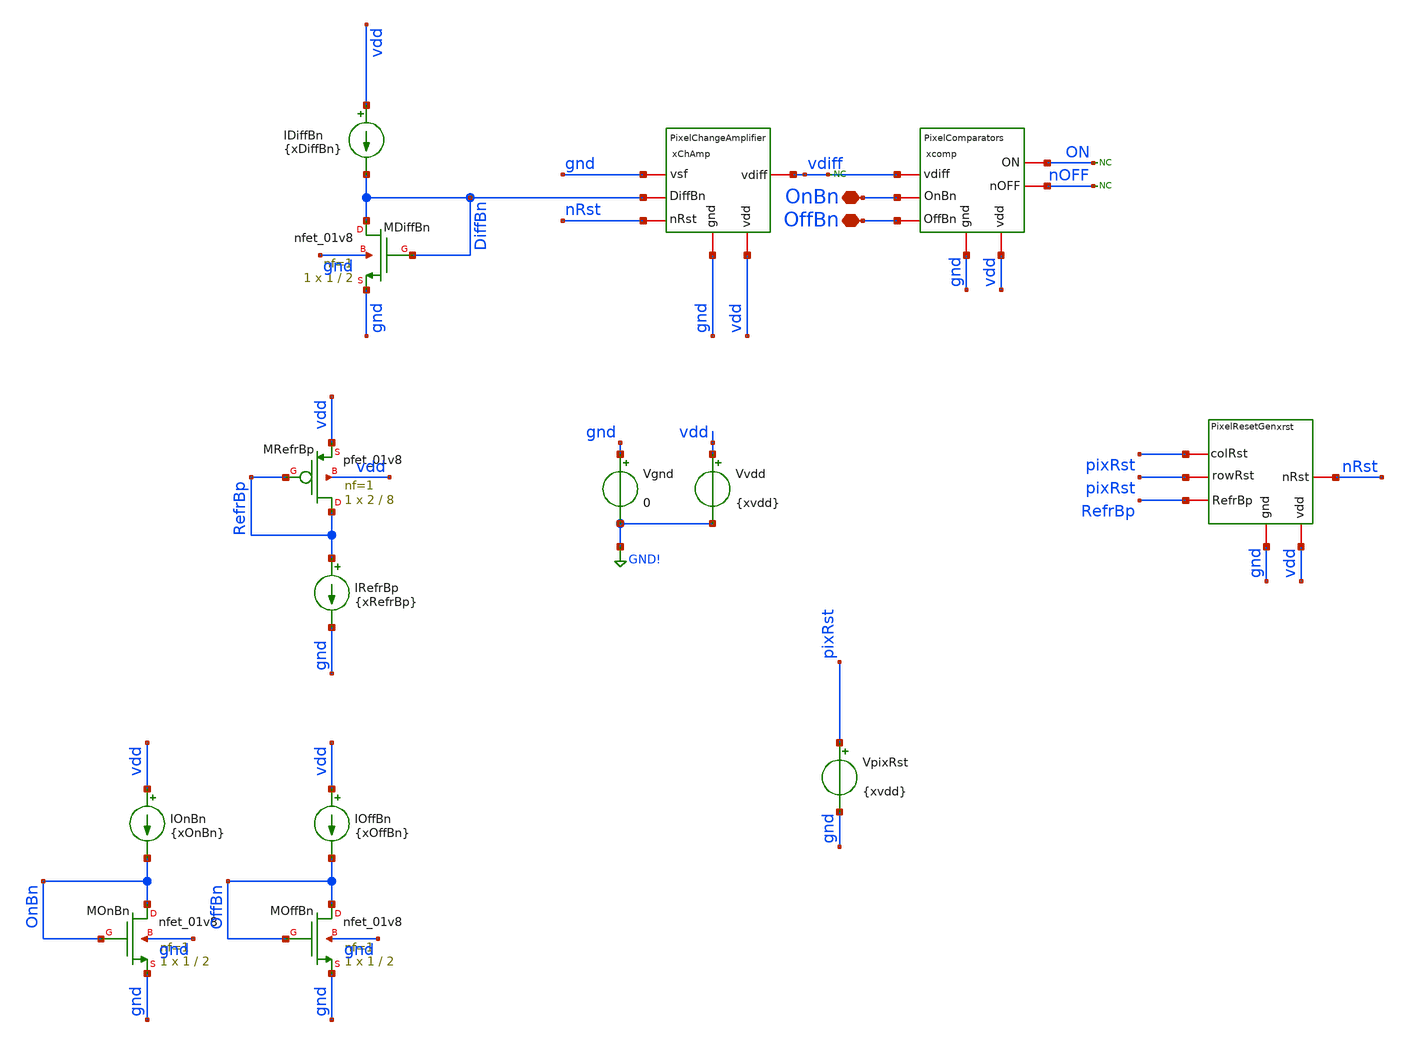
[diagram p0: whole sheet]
** sch_path: analog/xschem/tb_PixelReset_tran.sch
**.subckt tb_PixelReset_tran OnBn OffBn
*.iopin OnBn
*.iopin OffBn
Vgnd gnd GND! 0
Vvdd vdd GND! {xvdd}
xChAmp vdd DiffBn gnd gnd vdiff nRst PixelChangeAmplifier
XMDiffBn DiffBn DiffBn gnd gnd sky130_fd_pr__nfet_01v8 L=2 W=1 nf=1 ad='int((1 + 1)/2) * 1 / 1 * 0.29'
+ as='int((1 + 2)/2) * 1 / 1 * 0.29' pd='2*int((1 + 1)/2) * (1 / 1 + 0.29)' ps='2*int((1 + 2)/2) * (1 / 1 + 0.29)'
+ nrd='0.29 / 1 ' nrs='0.29 / 1 ' sa=0 sb=0 sd=0 mult=1 m=1
IDiffBn vdd DiffBn {xDiffBn}
* noconn vdiff
xcomp vdd OnBn gnd vdiff ON OffBn nOFF PixelComparators
xrst pixRst gnd pixRst nRst RefrBp vdd PixelResetGen
IRefrBp RefrBp gnd {xRefrBp}
XMRefrBp RefrBp RefrBp vdd vdd sky130_fd_pr__pfet_01v8 L=8 W=2 nf=1 ad='int((1 + 1)/2) * 2 / 1 * 0.29'
+ as='int((1 + 2)/2) * 2 / 1 * 0.29' pd='2*int((1 + 1)/2) * (2 / 1 + 0.29)' ps='2*int((1 + 2)/2) * (2 / 1 + 0.29)'
+ nrd='0.29 / 2 ' nrs='0.29 / 2 ' sa=0 sb=0 sd=0 mult=1 m=1
XMOnBn OnBn OnBn gnd gnd sky130_fd_pr__nfet_01v8 L=2 W=1 nf=1 ad='int((1 + 1)/2) * 1 / 1 * 0.29' as='int((1 + 2)/2) * 1 / 1 * 0.29'
+ pd='2*int((1 + 1)/2) * (1 / 1 + 0.29)' ps='2*int((1 + 2)/2) * (1 / 1 + 0.29)' nrd='0.29 / 1 ' nrs='0.29 / 1 '
+ sa=0 sb=0 sd=0 mult=1 m=1
IOnBn vdd OnBn {xOnBn}
XMOffBn OffBn OffBn gnd gnd sky130_fd_pr__nfet_01v8 L=2 W=1 nf=1 ad='int((1 + 1)/2) * 1 / 1 * 0.29' as='int((1 + 2)/2) * 1 / 1 * 0.29'
+ pd='2*int((1 + 1)/2) * (1 / 1 + 0.29)' ps='2*int((1 + 2)/2) * (1 / 1 + 0.29)' nrd='0.29 / 1 ' nrs='0.29 / 1 '
+ sa=0 sb=0 sd=0 mult=1 m=1
IOffBn vdd OffBn {xOffBn}
VpixRst pixRst gnd {xvdd}
* noconn ON
* noconn nOFF
**** begin user architecture code

** opencircuitdesign pdks install
.lib $::SKYWATER_MODELS/sky130.lib.spice tt



.temp 27

.option gmin=1e-16 abstol=1e-15 vntol=1e-9 reltol=1e-4 chgtol=1e-16
.option method=gear maxord=2 trtol=1
.option itl1=500 itl2=200 itl4=50
.option gminsteps=200 srcsteps=200

.param xvdd = 1.8
.param xRefrBp = 4n
.param xDiffBn = 10n
.param xOnBn = 100n
.param xOffBn = 1n

.param xvsf = 0.7

.save all
.save @m.xchamp.xmrst.msky130_fd_pr__pfet_01v8_hvt[id]
.save @m.xchamp.xmrst.msky130_fd_pr__pfet_01v8_hvt[ibd]
.save @m.xchamp.xmrst.msky130_fd_pr__pfet_01v8_hvt[ibs]
.save @m.xchamp.xmrst.msky130_fd_pr__pfet_01v8_hvt[igidl]
.save @m.xchamp.xmrst.msky130_fd_pr__pfet_01v8_hvt[igisl]

.control
** Phase 1: initial reset (VpixRst = xvdd from schematic)
stop when time > 1m
tran 100u 50 uic
let vdd_val = v(vdd)[length(v(vdd))-1]
echo
echo '=== Phase 1: initial reset complete (t=1ms) ==='

** Phase 2: release reset, run until ON fires
alter vpixrst = 0
delete all
let on_thresh = 0.9 * vdd_val
stop when v(on) > $&on_thresh
resume

let t_on_event = time[length(time)-1]
echo
echo '=== Phase 2: ON event detected ==='
print t_on_event

** Phase 3: trigger second reset for 10us
alter vpixrst = $&vdd_val
delete all
let t_rst2_end = t_on_event + 10u
stop when time > $&t_rst2_end
resume
echo
echo '=== Phase 3: second reset complete (10us pulse) ==='

** Phase 4: release second reset, run 0.5s more
alter vpixrst = 0
delete all
let t_final = t_on_event + 0.5
stop when time > $&t_final
resume
echo
echo '=== Phase 4: post-reset observation complete ==='

write tb_PixelReset_tran.raw
echo 'Raw file written. Running Python analysis...'
shell python3
+ /home/rpgraca/research/projects/telluride/2025/nic_eventcam/nic2025_openDVS/analog/xschem/tb_PixelReset_tran.py tb_PixelReset_tran.raw
.endc


**** end user architecture code
**.ends

* expanding   symbol:  PixelChangeAmplifier.sym # of pins=6
** sym_path: analog/xschem/PixelChangeAmplifier.sym
** sch_path: analog/xschem/PixelChangeAmplifier.sch
.subckt PixelChangeAmplifier vdd DiffBn gnd vsf vdiff nRst
*.iopin DiffBn
*.iopin vsf
*.iopin vdd
*.iopin gnd
*.iopin vdiff
*.iopin nRst
XC1 vsf vd sky130_fd_pr__cap_mim_m3_1 W=1 L=1 MF=40 m=40
XC2 vd vdiff sky130_fd_pr__cap_mim_m3_1 W=1 L=1 MF=2 m=2
XMchAmpBias vdiff DiffBn gnd gnd sky130_fd_pr__nfet_01v8 L=2 W=2 nf=1 ad='int((1 + 1)/2) * 2 / 1 * 0.29'
+ as='int((1 + 2)/2) * 2 / 1 * 0.29' pd='2*int((1 + 1)/2) * (2 / 1 + 0.29)' ps='2*int((1 + 2)/2) * (2 / 1 + 0.29)'
+ nrd='0.29 / 2 ' nrs='0.29 / 2 ' sa=0 sb=0 sd=0 mult=1 m=1
XMrst vdiff nRst vd vdd sky130_fd_pr__pfet_01v8_hvt L=0.3 W=1 nf=1 ad='int((1 + 1)/2) * 1 / 1 * 0.29'
+ as='int((1 + 2)/2) * 1 / 1 * 0.29' pd='2*int((1 + 1)/2) * (1 / 1 + 0.29)' ps='2*int((1 + 2)/2) * (1 / 1 + 0.29)'
+ nrd='0.29 / 1 ' nrs='0.29 / 1 ' sa=0 sb=0 sd=0 mult=1 m=1
XMchAmp vdiff vd vdd vdd sky130_fd_pr__pfet_01v8_hvt L=2 W=2 nf=1 ad='int((1 + 1)/2) * 2 / 1 * 0.29'
+ as='int((1 + 2)/2) * 2 / 1 * 0.29' pd='2*int((1 + 1)/2) * (2 / 1 + 0.29)' ps='2*int((1 + 2)/2) * (2 / 1 + 0.29)'
+ nrd='0.29 / 2 ' nrs='0.29 / 2 ' sa=0 sb=0 sd=0 mult=1 m=1
.ends


* expanding   symbol:  PixelComparators.sym # of pins=7
** sym_path: analog/xschem/PixelComparators.sym
** sch_path: analog/xschem/PixelComparators.sch
.subckt PixelComparators vdd OnBn gnd vdiff ON OffBn nOFF
*.iopin OnBn
*.iopin OffBn
*.iopin vdd
*.iopin vdiff
*.iopin gnd
*.iopin ON
*.iopin nOFF
XMonBias ON OnBn gnd gnd sky130_fd_pr__nfet_01v8 L=2 W=2 nf=1 ad='int((1 + 1)/2) * 2 / 1 * 0.29' as='int((1 + 2)/2) * 2 / 1 * 0.29'
+ pd='2*int((1 + 1)/2) * (2 / 1 + 0.29)' ps='2*int((1 + 2)/2) * (2 / 1 + 0.29)' nrd='0.29 / 2 ' nrs='0.29 / 2 '
+ sa=0 sb=0 sd=0 mult=1 m=1
XMoffBias nOFF OffBn gnd gnd sky130_fd_pr__nfet_01v8 L=2 W=2 nf=1 ad='int((1 + 1)/2) * 2 / 1 * 0.29'
+ as='int((1 + 2)/2) * 2 / 1 * 0.29' pd='2*int((1 + 1)/2) * (2 / 1 + 0.29)' ps='2*int((1 + 2)/2) * (2 / 1 + 0.29)'
+ nrd='0.29 / 2 ' nrs='0.29 / 2 ' sa=0 sb=0 sd=0 mult=1 m=1
XMon ON vdiff vdd vdd sky130_fd_pr__pfet_01v8_hvt L=2 W=2 nf=1 ad='int((1 + 1)/2) * 2 / 1 * 0.29' as='int((1 + 2)/2) * 2 / 1 * 0.29'
+ pd='2*int((1 + 1)/2) * (2 / 1 + 0.29)' ps='2*int((1 + 2)/2) * (2 / 1 + 0.29)' nrd='0.29 / 2 ' nrs='0.29 / 2 '
+ sa=0 sb=0 sd=0 mult=1 m=1
XMoff nOFF vdiff vdd vdd sky130_fd_pr__pfet_01v8_hvt L=2 W=2 nf=1 ad='int((1 + 1)/2) * 2 / 1 * 0.29'
+ as='int((1 + 2)/2) * 2 / 1 * 0.29' pd='2*int((1 + 1)/2) * (2 / 1 + 0.29)' ps='2*int((1 + 2)/2) * (2 / 1 + 0.29)'
+ nrd='0.29 / 2 ' nrs='0.29 / 2 ' sa=0 sb=0 sd=0 mult=1 m=1
.ends


* expanding   symbol:  PixelResetGen.sym # of pins=6
** sym_path: analog/xschem/PixelResetGen.sym
** sch_path: analog/xschem/PixelResetGen.sch
.subckt PixelResetGen rowRst gnd colRst nRst RefrBp vdd
*.ipin rowRst
*.ipin colRst
*.iopin RefrBp
*.iopin gnd
*.iopin vdd
*.iopin nRst
XMrefrInv nRst colRst net1 gnd sky130_fd_pr__nfet_01v8 L=0.15 W=0.5 nf=1 ad='int((1 + 1)/2) * 0.5 / 1 * 0.29'
+ as='int((1 + 2)/2) * 0.5 / 1 * 0.29' pd='2*int((1 + 1)/2) * (0.5 / 1 + 0.29)' ps='2*int((1 + 2)/2) * (0.5 / 1 + 0.29)'
+ nrd='0.29 / 0.5 ' nrs='0.29 / 0.5 ' sa=0 sb=0 sd=0 mult=1 m=1
XMrefrBias nRst RefrBp vdd vdd sky130_fd_pr__pfet_01v8 L=8 W=2 nf=1 ad='int((1 + 1)/2) * 2 / 1 * 0.29'
+ as='int((1 + 2)/2) * 2 / 1 * 0.29' pd='2*int((1 + 1)/2) * (2 / 1 + 0.29)' ps='2*int((1 + 2)/2) * (2 / 1 + 0.29)'
+ nrd='0.29 / 2 ' nrs='0.29 / 2 ' sa=0 sb=0 sd=0 mult=1 m=1
XMcapRefr vdd nRst vdd vdd sky130_fd_pr__pfet_01v8_hvt L=8 W=8 nf=1 ad='int((1 + 1)/2) * 8 / 1 * 0.29'
+ as='int((1 + 2)/2) * 8 / 1 * 0.29' pd='2*int((1 + 1)/2) * (8 / 1 + 0.29)' ps='2*int((1 + 2)/2) * (8 / 1 + 0.29)'
+ nrd='0.29 / 8 ' nrs='0.29 / 8 ' sa=0 sb=0 sd=0 mult=1 m=1
XMswON1 net1 rowRst gnd gnd sky130_fd_pr__nfet_01v8 L=0.15 W=0.5 nf=1 ad='int((1 + 1)/2) * 0.5 / 1 * 0.29'
+ as='int((1 + 2)/2) * 0.5 / 1 * 0.29' pd='2*int((1 + 1)/2) * (0.5 / 1 + 0.29)' ps='2*int((1 + 2)/2) * (0.5 / 1 + 0.29)'
+ nrd='0.29 / 0.5 ' nrs='0.29 / 0.5 ' sa=0 sb=0 sd=0 mult=1 m=1
.ends

.GLOBAL GND!
.end
